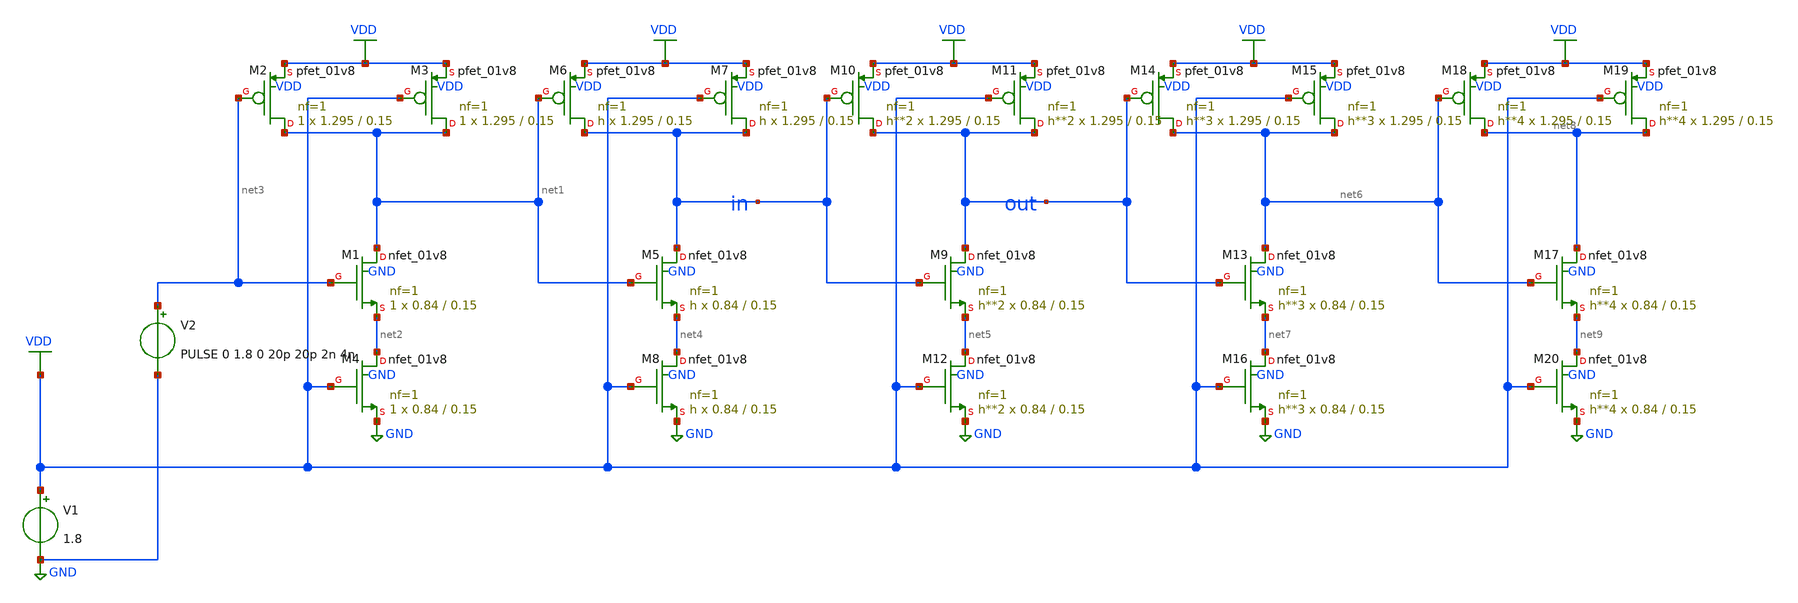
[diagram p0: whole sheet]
** sch_path: logicaleffort/nand2.sch
**.subckt nand2
XM1 net1 net3 net2 GND sky130_fd_pr__nfet_01v8 L=0.15 W=0.84 nf=1 ad='int((1 + 1)/2) * 0.84 / 1 * 0.29'
+ as='int((1 + 2)/2) * 0.84 / 1 * 0.29' pd='2*int((1 + 1)/2) * (0.84 / 1 + 0.29)' ps='2*int((1 + 2)/2) * (0.84 / 1 + 0.29)'
+ nrd='0.29 / 0.84 ' nrs='0.29 / 0.84 ' sa=0 sb=0 sd=0 mult=1 m=1
XM2 net1 net3 VDD VDD sky130_fd_pr__pfet_01v8 L=0.15 W=1.295 nf=1 ad='int((1 + 1)/2) * 1.295 / 1 * 0.29'
+ as='int((1 + 2)/2) * 1.295 / 1 * 0.29' pd='2*int((1 + 1)/2) * (1.295 / 1 + 0.29)' ps='2*int((1 + 2)/2) * (1.295 / 1 + 0.29)'
+ nrd='0.29 / 1.295 ' nrs='0.29 / 1.295 ' sa=0 sb=0 sd=0 mult=1 m=1
XM3 net1 VDD VDD VDD sky130_fd_pr__pfet_01v8 L=0.15 W=1.295 nf=1 ad='int((1 + 1)/2) * 1.295 / 1 * 0.29'
+ as='int((1 + 2)/2) * 1.295 / 1 * 0.29' pd='2*int((1 + 1)/2) * (1.295 / 1 + 0.29)' ps='2*int((1 + 2)/2) * (1.295 / 1 + 0.29)'
+ nrd='0.29 / 1.295 ' nrs='0.29 / 1.295 ' sa=0 sb=0 sd=0 mult=1 m=1
XM4 net2 VDD GND GND sky130_fd_pr__nfet_01v8 L=0.15 W=0.84 nf=1 ad='int((1 + 1)/2) * 0.84 / 1 * 0.29'
+ as='int((1 + 2)/2) * 0.84 / 1 * 0.29' pd='2*int((1 + 1)/2) * (0.84 / 1 + 0.29)' ps='2*int((1 + 2)/2) * (0.84 / 1 + 0.29)'
+ nrd='0.29 / 0.84 ' nrs='0.29 / 0.84 ' sa=0 sb=0 sd=0 mult=1 m=1
XM5 in net1 net4 GND sky130_fd_pr__nfet_01v8 L=0.15 W=0.84 nf=1 ad='int((1 + 1)/2) * 0.84 / 1 * 0.29'
+ as='int((1 + 2)/2) * 0.84 / 1 * 0.29' pd='2*int((1 + 1)/2) * (0.84 / 1 + 0.29)' ps='2*int((1 + 2)/2) * (0.84 / 1 + 0.29)'
+ nrd='0.29 / 0.84 ' nrs='0.29 / 0.84 ' sa=0 sb=0 sd=0 mult=h m=h
XM6 in net1 VDD VDD sky130_fd_pr__pfet_01v8 L=0.15 W=1.295 nf=1 ad='int((1 + 1)/2) * 1.295 / 1 * 0.29'
+ as='int((1 + 2)/2) * 1.295 / 1 * 0.29' pd='2*int((1 + 1)/2) * (1.295 / 1 + 0.29)' ps='2*int((1 + 2)/2) * (1.295 / 1 + 0.29)'
+ nrd='0.29 / 1.295 ' nrs='0.29 / 1.295 ' sa=0 sb=0 sd=0 mult=h m=h
XM7 in VDD VDD VDD sky130_fd_pr__pfet_01v8 L=0.15 W=1.295 nf=1 ad='int((1 + 1)/2) * 1.295 / 1 * 0.29'
+ as='int((1 + 2)/2) * 1.295 / 1 * 0.29' pd='2*int((1 + 1)/2) * (1.295 / 1 + 0.29)' ps='2*int((1 + 2)/2) * (1.295 / 1 + 0.29)'
+ nrd='0.29 / 1.295 ' nrs='0.29 / 1.295 ' sa=0 sb=0 sd=0 mult=h m=h
XM8 net4 VDD GND GND sky130_fd_pr__nfet_01v8 L=0.15 W=0.84 nf=1 ad='int((1 + 1)/2) * 0.84 / 1 * 0.29'
+ as='int((1 + 2)/2) * 0.84 / 1 * 0.29' pd='2*int((1 + 1)/2) * (0.84 / 1 + 0.29)' ps='2*int((1 + 2)/2) * (0.84 / 1 + 0.29)'
+ nrd='0.29 / 0.84 ' nrs='0.29 / 0.84 ' sa=0 sb=0 sd=0 mult=h m=h
XM9 out in net5 GND sky130_fd_pr__nfet_01v8 L=0.15 W=0.84 nf=1 ad='int((1 + 1)/2) * 0.84 / 1 * 0.29'
+ as='int((1 + 2)/2) * 0.84 / 1 * 0.29' pd='2*int((1 + 1)/2) * (0.84 / 1 + 0.29)' ps='2*int((1 + 2)/2) * (0.84 / 1 + 0.29)'
+ nrd='0.29 / 0.84 ' nrs='0.29 / 0.84 ' sa=0 sb=0 sd=0 mult=h**2 m=h**2
XM10 out in VDD VDD sky130_fd_pr__pfet_01v8 L=0.15 W=1.295 nf=1 ad='int((1 + 1)/2) * 1.295 / 1 * 0.29'
+ as='int((1 + 2)/2) * 1.295 / 1 * 0.29' pd='2*int((1 + 1)/2) * (1.295 / 1 + 0.29)' ps='2*int((1 + 2)/2) * (1.295 / 1 + 0.29)'
+ nrd='0.29 / 1.295 ' nrs='0.29 / 1.295 ' sa=0 sb=0 sd=0 mult=h**2 m=h**2
XM11 out VDD VDD VDD sky130_fd_pr__pfet_01v8 L=0.15 W=1.295 nf=1 ad='int((1 + 1)/2) * 1.295 / 1 * 0.29'
+ as='int((1 + 2)/2) * 1.295 / 1 * 0.29' pd='2*int((1 + 1)/2) * (1.295 / 1 + 0.29)' ps='2*int((1 + 2)/2) * (1.295 / 1 + 0.29)'
+ nrd='0.29 / 1.295 ' nrs='0.29 / 1.295 ' sa=0 sb=0 sd=0 mult=h**2 m=h**2
XM12 net5 VDD GND GND sky130_fd_pr__nfet_01v8 L=0.15 W=0.84 nf=1 ad='int((1 + 1)/2) * 0.84 / 1 * 0.29'
+ as='int((1 + 2)/2) * 0.84 / 1 * 0.29' pd='2*int((1 + 1)/2) * (0.84 / 1 + 0.29)' ps='2*int((1 + 2)/2) * (0.84 / 1 + 0.29)'
+ nrd='0.29 / 0.84 ' nrs='0.29 / 0.84 ' sa=0 sb=0 sd=0 mult=h**2 m=h**2
XM13 net6 out net7 GND sky130_fd_pr__nfet_01v8 L=0.15 W=0.84 nf=1 ad='int((1 + 1)/2) * 0.84 / 1 * 0.29'
+ as='int((1 + 2)/2) * 0.84 / 1 * 0.29' pd='2*int((1 + 1)/2) * (0.84 / 1 + 0.29)' ps='2*int((1 + 2)/2) * (0.84 / 1 + 0.29)'
+ nrd='0.29 / 0.84 ' nrs='0.29 / 0.84 ' sa=0 sb=0 sd=0 mult=h**3 m=h**3
XM14 net6 out VDD VDD sky130_fd_pr__pfet_01v8 L=0.15 W=1.295 nf=1 ad='int((1 + 1)/2) * 1.295 / 1 * 0.29'
+ as='int((1 + 2)/2) * 1.295 / 1 * 0.29' pd='2*int((1 + 1)/2) * (1.295 / 1 + 0.29)' ps='2*int((1 + 2)/2) * (1.295 / 1 + 0.29)'
+ nrd='0.29 / 1.295 ' nrs='0.29 / 1.295 ' sa=0 sb=0 sd=0 mult=h**3 m=h**3
XM15 net6 VDD VDD VDD sky130_fd_pr__pfet_01v8 L=0.15 W=1.295 nf=1 ad='int((1 + 1)/2) * 1.295 / 1 * 0.29'
+ as='int((1 + 2)/2) * 1.295 / 1 * 0.29' pd='2*int((1 + 1)/2) * (1.295 / 1 + 0.29)' ps='2*int((1 + 2)/2) * (1.295 / 1 + 0.29)'
+ nrd='0.29 / 1.295 ' nrs='0.29 / 1.295 ' sa=0 sb=0 sd=0 mult=h**3 m=h**3
XM16 net7 VDD GND GND sky130_fd_pr__nfet_01v8 L=0.15 W=0.84 nf=1 ad='int((1 + 1)/2) * 0.84 / 1 * 0.29'
+ as='int((1 + 2)/2) * 0.84 / 1 * 0.29' pd='2*int((1 + 1)/2) * (0.84 / 1 + 0.29)' ps='2*int((1 + 2)/2) * (0.84 / 1 + 0.29)'
+ nrd='0.29 / 0.84 ' nrs='0.29 / 0.84 ' sa=0 sb=0 sd=0 mult=h**3 m=h**3
XM17 net8 net6 net9 GND sky130_fd_pr__nfet_01v8 L=0.15 W=0.84 nf=1 ad='int((1 + 1)/2) * 0.84 / 1 * 0.29'
+ as='int((1 + 2)/2) * 0.84 / 1 * 0.29' pd='2*int((1 + 1)/2) * (0.84 / 1 + 0.29)' ps='2*int((1 + 2)/2) * (0.84 / 1 + 0.29)'
+ nrd='0.29 / 0.84 ' nrs='0.29 / 0.84 ' sa=0 sb=0 sd=0 mult=h**4 m=h**4
XM18 net8 net6 VDD VDD sky130_fd_pr__pfet_01v8 L=0.15 W=1.295 nf=1 ad='int((1 + 1)/2) * 1.295 / 1 * 0.29'
+ as='int((1 + 2)/2) * 1.295 / 1 * 0.29' pd='2*int((1 + 1)/2) * (1.295 / 1 + 0.29)' ps='2*int((1 + 2)/2) * (1.295 / 1 + 0.29)'
+ nrd='0.29 / 1.295 ' nrs='0.29 / 1.295 ' sa=0 sb=0 sd=0 mult=h**4 m=h**4
XM19 net8 VDD VDD VDD sky130_fd_pr__pfet_01v8 L=0.15 W=1.295 nf=1 ad='int((1 + 1)/2) * 1.295 / 1 * 0.29'
+ as='int((1 + 2)/2) * 1.295 / 1 * 0.29' pd='2*int((1 + 1)/2) * (1.295 / 1 + 0.29)' ps='2*int((1 + 2)/2) * (1.295 / 1 + 0.29)'
+ nrd='0.29 / 1.295 ' nrs='0.29 / 1.295 ' sa=0 sb=0 sd=0 mult=h**4 m=h**4
XM20 net9 VDD GND GND sky130_fd_pr__nfet_01v8 L=0.15 W=0.84 nf=1 ad='int((1 + 1)/2) * 0.84 / 1 * 0.29'
+ as='int((1 + 2)/2) * 0.84 / 1 * 0.29' pd='2*int((1 + 1)/2) * (0.84 / 1 + 0.29)' ps='2*int((1 + 2)/2) * (0.84 / 1 + 0.29)'
+ nrd='0.29 / 0.84 ' nrs='0.29 / 0.84 ' sa=0 sb=0 sd=0 mult=h**4 m=h**4
V1 VDD GND 1.8
V2 net3 GND PULSE 0 1.8 0 20p 20p 2n 4n
**** begin user architecture code


.lib /usr/local/share/pdk/sky130A/libs.tech/ngspice/sky130.lib.spice tt

.param h = 4
.control
  save in out
  let start = 1
  let stop = 8
  let step = 1
  let cur = start
  let n = ((stop - start) / step) + 1
  let hall = unitvec(n)
  let tpdrall = unitvec(n)
  let tpdfall = unitvec(n)
  let tpdall = unitvec(n)
  let diffall = unitvec(n)
  let m = 0
  while m < n
    let hv = cur
    alterparam h = $&hv
    reset
    tran 0.1p 20n
    meas tran tpdr trig v(in) val=0.9 fall=1 targ v(out) val=0.9 rise=1
    meas tran tpdf trig v(in) val=0.9 rise=1 targ v(out) val=0.9 fall=1
    let hall[m] = hv
    let tpdrall[m] = tpdr
    let tpdfall[m] = tpdf
    let tpdall[m] = (tpdr + tpdf) / 2
    let diffall[m] = abs(tpdr - tpdf)
    let cur = cur + step
    let m = m + 1
  end
  meas tran tr trig v(in) val = 0.18 rise=1 targ v(in) val=1.62 rise=1
  meas tran tf trig v(in) val = 1.62 fall=1 targ v(in) val=0.18 fall=1
  print hall tpdrall tpdfall tpdall diffall
.endc


**** end user architecture code
**.ends
.GLOBAL GND
.GLOBAL VDD
.end
